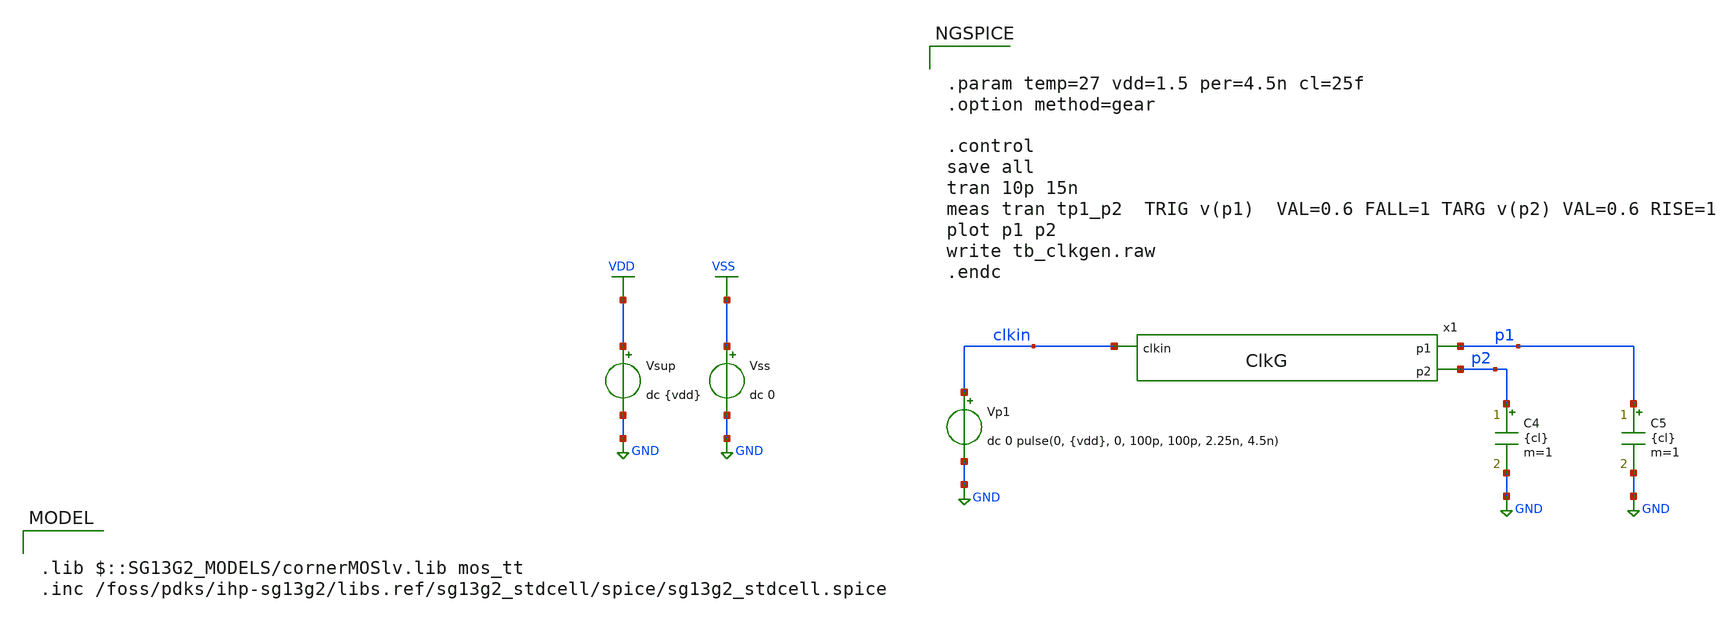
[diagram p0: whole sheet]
** sch_path: DSM/Schematics/Ideal_Circuits/Clock/tb_ClkG.sch
**.subckt tb_ClkG
Vsup VDD GND dc {vdd}
Vss VSS GND dc 0
x1 p1 clkin p2 ClkG
Vp1 clkin GND dc 0 pulse(0, {vdd}, 0, 100p, 100p, 2.25n, 4.5n)
C4 p2 GND {cl} m=1
C5 p1 GND {cl} m=1
**** begin user architecture code


.param temp=27 vdd=1.5 per=4.5n cl=25f
.option method=gear

.control
save all
tran 10p 15n
meas tran tp1_p2  TRIG v(p1)  VAL=0.6 FALL=1 TARG v(p2) VAL=0.6 RISE=1
plot p1 p2
write tb_clkgen.raw
.endc



.lib $::SG13G2_MODELS/cornerMOSlv.lib mos_tt
.inc /foss/pdks/ihp-sg13g2/libs.ref/sg13g2_stdcell/spice/sg13g2_stdcell.spice

**** end user architecture code
**.ends
.GLOBAL GND
.GLOBAL VDD
.GLOBAL VSS
.end
